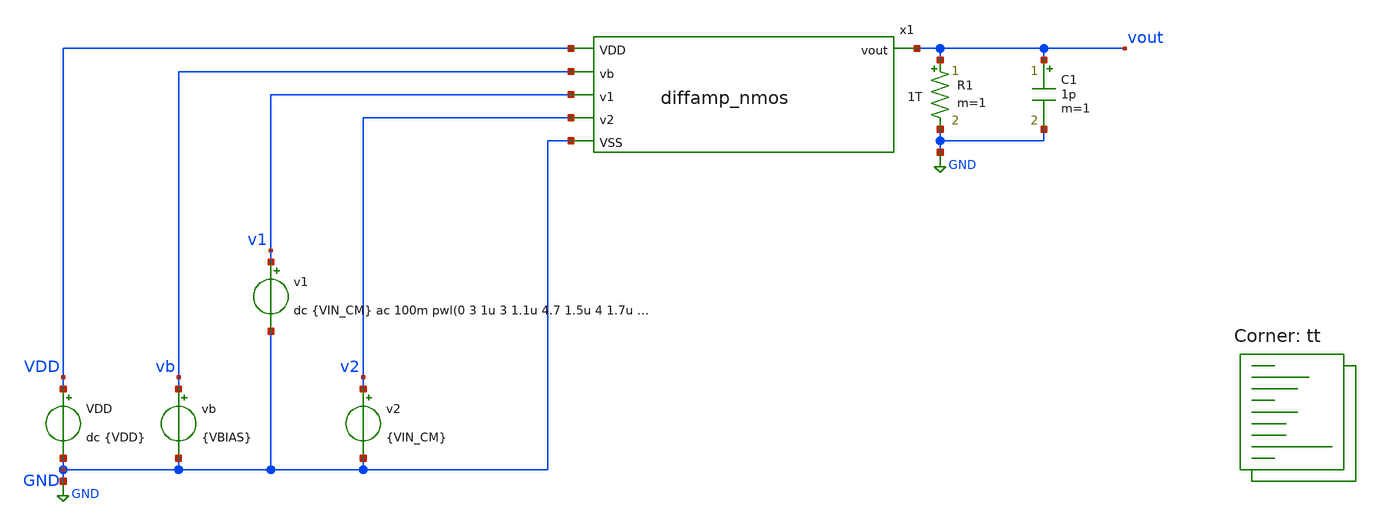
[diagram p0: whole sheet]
** sch_path: xschem/test_diffamp_nmos_ac.sch
**.subckt test_diffamp_nmos_ac
VDD VDD GND dc {VDD}
vb vb GND {VBIAS}
v1 v1 GND dc {VIN_CM} ac 100m pwl(0 3 1u 3 1.1u 4.7 1.5u 4 1.7u 0.5 2u 0.1 2.1u 3)
v2 v2 GND {VIN_CM}
R1 vout GND 1T m=1
x1 v1 v2 GND VDD vb vout diffamp_nmos
C1 vout GND 1p m=1
**** begin user architecture code
.lib $::SKYWATER_MODELS/sky130.lib.spice tt



.options reltol=0.0001 abstol=10e-15
*.include diffamp_nmos.spice
.param VDD=5
.param VSS=0
.param VBIAS=1
.param VIN_CM=3
.options savecurrents
* .options reltol=0.01 abstol=10e-12
.control
  save all
  op
  remzerovec
  write test_diffamp_nmos_ac.raw
  set appendwrite
  * ac sweep
  ac dec 10 100 100meg
  remzerovec
  write test_diffamp_nmos_ac.raw
.endc



**** end user architecture code
**.ends

* expanding   symbol:  diffamp_nmos.sym # of pins=6
** sym_path: xschem/diffamp_nmos.sym
** sch_path: xschem/diffamp_nmos.sch
.subckt diffamp_nmos v1 v2 VSS VDD vb vout
*.ipin v1
*.ipin v2
*.ipin vb
*.opin vout
*.ipin VDD
*.ipin VSS
XM7 int2 int3 VDD VDD sky130_fd_pr__pfet_g5v0d10v5 L=1 W=1.5 nf=1 ad='int((nf+1)/2) * W/nf * 0.29' as='int((nf+2)/2) * W/nf * 0.29'
+ pd='2*int((nf+1)/2) * (W/nf + 0.29)' ps='2*int((nf+2)/2) * (W/nf + 0.29)' nrd='0.29 / W' nrs='0.29 / W'
+ sa=0 sb=0 sd=0 mult=1 m=1
XM8 int2 int2 VSS VSS sky130_fd_pr__nfet_g5v0d10v5 L=1 W=1.5 nf=1 ad='int((nf+1)/2) * W/nf * 0.29' as='int((nf+2)/2) * W/nf * 0.29'
+ pd='2*int((nf+1)/2) * (W/nf + 0.29)' ps='2*int((nf+2)/2) * (W/nf + 0.29)' nrd='0.29 / W' nrs='0.29 / W'
+ sa=0 sb=0 sd=0 mult=1 m=1
XM9 vout int2 VSS VSS sky130_fd_pr__nfet_g5v0d10v5 L=1 W=1.5 nf=1 ad='int((nf+1)/2) * W/nf * 0.29' as='int((nf+2)/2) * W/nf * 0.29'
+ pd='2*int((nf+1)/2) * (W/nf + 0.29)' ps='2*int((nf+2)/2) * (W/nf + 0.29)' nrd='0.29 / W' nrs='0.29 / W'
+ sa=0 sb=0 sd=0 mult=1 m=1
XM1 int4 v1 int1 VSS sky130_fd_pr__nfet_g5v0d10v5 L=1 W=1.5 nf=1 ad='int((nf+1)/2) * W/nf * 0.29' as='int((nf+2)/2) * W/nf * 0.29'
+ pd='2*int((nf+1)/2) * (W/nf + 0.29)' ps='2*int((nf+2)/2) * (W/nf + 0.29)' nrd='0.29 / W' nrs='0.29 / W'
+ sa=0 sb=0 sd=0 mult=1 m=1
XM2 int3 v2 int1 VSS sky130_fd_pr__nfet_g5v0d10v5 L=1 W=1.5 nf=1 ad='int((nf+1)/2) * W/nf * 0.29' as='int((nf+2)/2) * W/nf * 0.29'
+ pd='2*int((nf+1)/2) * (W/nf + 0.29)' ps='2*int((nf+2)/2) * (W/nf + 0.29)' nrd='0.29 / W' nrs='0.29 / W'
+ sa=0 sb=0 sd=0 mult=1 m=1
XM6 int3 int3 VDD VDD sky130_fd_pr__pfet_g5v0d10v5 L=1 W=1.5 nf=1 ad='int((nf+1)/2) * W/nf * 0.29' as='int((nf+2)/2) * W/nf * 0.29'
+ pd='2*int((nf+1)/2) * (W/nf + 0.29)' ps='2*int((nf+2)/2) * (W/nf + 0.29)' nrd='0.29 / W' nrs='0.29 / W'
+ sa=0 sb=0 sd=0 mult=1 m=1
XM5 vout int4 VDD VDD sky130_fd_pr__pfet_g5v0d10v5 L=1 W=1.5 nf=1 ad='int((nf+1)/2) * W/nf * 0.29' as='int((nf+2)/2) * W/nf * 0.29'
+ pd='2*int((nf+1)/2) * (W/nf + 0.29)' ps='2*int((nf+2)/2) * (W/nf + 0.29)' nrd='0.29 / W' nrs='0.29 / W'
+ sa=0 sb=0 sd=0 mult=1 m=1
XM3a int1 vb int5 VSS sky130_fd_pr__nfet_g5v0d10v5 L=1 W=1.5 nf=1 ad='int((nf+1)/2) * W/nf * 0.29' as='int((nf+2)/2) * W/nf * 0.29'
+ pd='2*int((nf+1)/2) * (W/nf + 0.29)' ps='2*int((nf+2)/2) * (W/nf + 0.29)' nrd='0.29 / W' nrs='0.29 / W'
+ sa=0 sb=0 sd=0 mult=1 m=1
XM3b int5 vb VSS VSS sky130_fd_pr__nfet_g5v0d10v5 L=1 W=1.5 nf=1 ad='int((nf+1)/2) * W/nf * 0.29' as='int((nf+2)/2) * W/nf * 0.29'
+ pd='2*int((nf+1)/2) * (W/nf + 0.29)' ps='2*int((nf+2)/2) * (W/nf + 0.29)' nrd='0.29 / W' nrs='0.29 / W'
+ sa=0 sb=0 sd=0 mult=1 m=1
XM4 int4 int4 VDD VDD sky130_fd_pr__pfet_g5v0d10v5 L=1 W=1.5 nf=1 ad='int((nf+1)/2) * W/nf * 0.29' as='int((nf+2)/2) * W/nf * 0.29'
+ pd='2*int((nf+1)/2) * (W/nf + 0.29)' ps='2*int((nf+2)/2) * (W/nf + 0.29)' nrd='0.29 / W' nrs='0.29 / W'
+ sa=0 sb=0 sd=0 mult=1 m=1
.ends

.GLOBAL GND
.end
